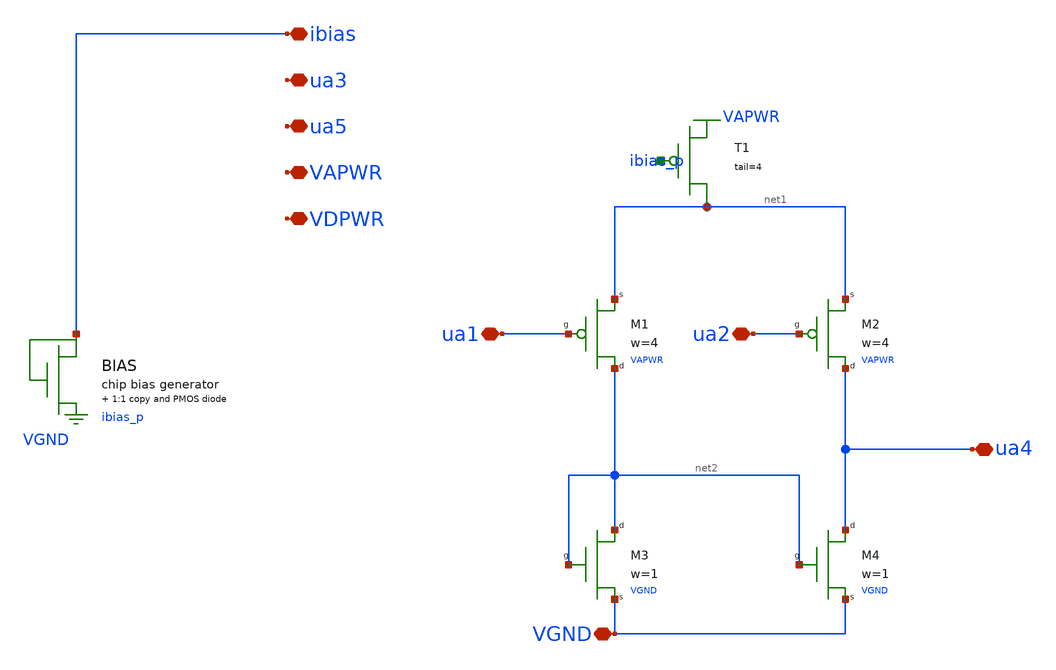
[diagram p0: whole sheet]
** sch_path: examples/pdiffamp/pdiffamp.sch
**.subckt pdiffamp ibias ua1 ua2 ua3 ua4 ua5 VAPWR VDPWR VGND
*.iopin ibias
*.iopin ua1
*.iopin ua2
*.iopin ua3
*.iopin ua4
*.iopin ua5
*.iopin VAPWR
*.iopin VDPWR
*.iopin VGND
M1 ua1 net2 net1 VAPWR mosbius_pmos w=4
M2 ua2 ua4 net1 VAPWR mosbius_pmos w=4
XT1 net1 ibias_p VAPWR mosbius_ptail tail=4
XM3 net2 net2 VGND VGND mosbius_nmos w=1
XM4 net2 ua4 VGND VGND mosbius_nmos w=1
XBIAS ibias ibias_p VGND VAPWR mosbius_bias
**.ends

* expanding   symbol:  mosbius_pmos.sym # of pins=3
** sym_path: xschem/mosbius_lib/mosbius_pmos.sym
** sch_path: xschem/mosbius_lib/mosbius_pmos.sch
.subckt mosbius_pmos g d s b  w=1
*.iopin s
*.ipin g
*.iopin d
XM1 d g s b sky130_fd_pr__pfet_g5v0d10v5 L=0.5 W=wdev nf=nfdev ad='int((nf+1)/2) * W/nf * 0.29' as='int((nf+2)/2) * W/nf * 0.29'
+ pd='2*int((nf+1)/2) * (W/nf + 0.29)' ps='2*int((nf+2)/2) * (W/nf + 0.29)' nrd='0.29 / W' nrs='0.29 / W'
+ sa=0 sb=0 sd=0 mult=1 m=1
**** begin user architecture code

.param wdev='30*w' nfdev='4*w'

**** end user architecture code
.ends


* expanding   symbol:  mosbius_ptail.sym # of pins=1
** sym_path: xschem/mosbius_lib/mosbius_ptail.sym
** sch_path: xschem/mosbius_lib/mosbius_ptail.sch
.subckt mosbius_ptail d g s  tail=2
*.iopin d
XM2 d g s s sky130_fd_pr__pfet_g5v0d10v5 L=1 W=60*(tail/2) nf=60*(tail/2)/pmos_width_per_finger ad='int((nf+1)/2) * W/nf * 0.29'
+ as='int((nf+2)/2) * W/nf * 0.29' pd='2*int((nf+1)/2) * (W/nf + 0.29)' ps='2*int((nf+2)/2) * (W/nf + 0.29)'
+ nrd='0.29 / W' nrs='0.29 / W' sa=0 sb=0 sd=0 mult=1 m=1
* implicit port xxx
* implicit port xxx
.ends


* expanding   symbol:  mosbius_nmos.sym # of pins=3
** sym_path: xschem/mosbius_lib/mosbius_nmos.sym
** sch_path: xschem/mosbius_lib/mosbius_nmos.sch
.subckt mosbius_nmos g d s b  w=1
*.iopin s
*.ipin g
*.iopin d
XM1 d g s b sky130_fd_pr__nfet_g5v0d10v5 L=0.5 W=wdev nf=nfdev ad='int((nf+1)/2) * W/nf * 0.29' as='int((nf+2)/2) * W/nf * 0.29'
+ pd='2*int((nf+1)/2) * (W/nf + 0.29)' ps='2*int((nf+2)/2) * (W/nf + 0.29)' nrd='0.29 / W' nrs='0.29 / W'
+ sa=0 sb=0 sd=0 mult=1 m=1
**** begin user architecture code

.param wdev='10*w' nfdev='2*w'

**** end user architecture code
.ends


* expanding   symbol:  mosbius_bias.sym # of pins=1
** sym_path: xschem/mosbius_lib/mosbius_bias.sym
** sch_path: xschem/mosbius_lib/mosbius_bias.sch
.subckt mosbius_bias ibias ibias_p bn bp
*.iopin ibias
XMbias_ref ibias ibias bn bn sky130_fd_pr__nfet_g5v0d10v5 L=1 W=10 nf=2 ad='int((nf+1)/2) * W/nf * 0.29'
+ as='int((nf+2)/2) * W/nf * 0.29' pd='2*int((nf+1)/2) * (W/nf + 0.29)' ps='2*int((nf+2)/2) * (W/nf + 0.29)'
+ nrd='0.29 / W' nrs='0.29 / W' sa=0 sb=0 sd=0 mult=1 m=1
XMbias_copy ibias_p ibias bn bn sky130_fd_pr__nfet_g5v0d10v5 L=1 W=10 nf=2 ad='int((nf+1)/2) * W/nf * 0.29'
+ as='int((nf+2)/2) * W/nf * 0.29' pd='2*int((nf+1)/2) * (W/nf + 0.29)' ps='2*int((nf+2)/2) * (W/nf + 0.29)'
+ nrd='0.29 / W' nrs='0.29 / W' sa=0 sb=0 sd=0 mult=1 m=1
XMbias_p ibias_p ibias_p bp bp sky130_fd_pr__pfet_g5v0d10v5 L=1 W=30 nf=30/pmos_width_per_finger ad='int((nf+1)/2) * W/nf * 0.29'
+ as='int((nf+2)/2) * W/nf * 0.29' pd='2*int((nf+1)/2) * (W/nf + 0.29)' ps='2*int((nf+2)/2) * (W/nf + 0.29)'
+ nrd='0.29 / W' nrs='0.29 / W' sa=0 sb=0 sd=0 mult=1 m=1
* implicit port xxx
.ends

.end
